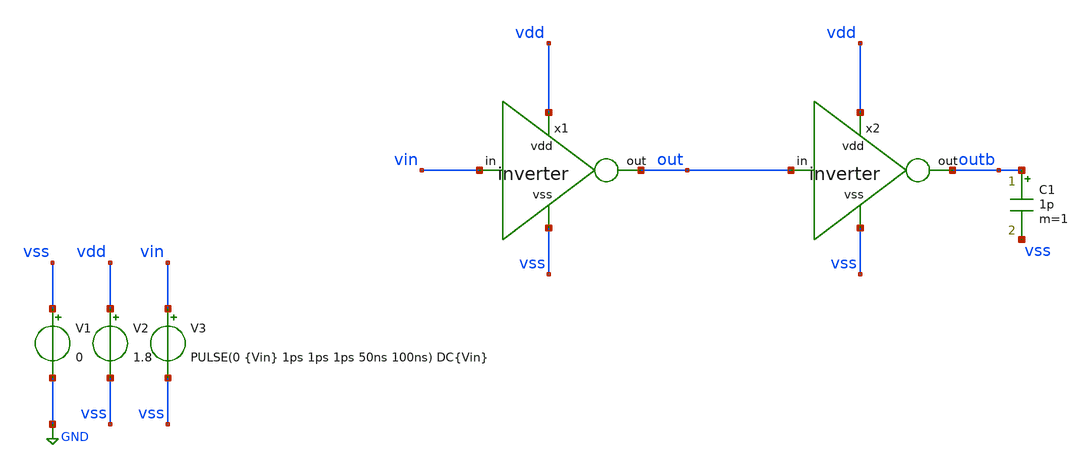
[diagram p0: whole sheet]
** sch_path: track_vlsi/ledesma/sch/tb_inverter.sch
**.subckt tb_inverter
x1 vdd out vin vss inverter
V1 vss GND 0
V2 vdd vss 1.8
V3 vin vss PULSE(0 {Vin} 1ps 1ps 1ps 50ns 100ns) DC{Vin}
x2 vdd outb out vss inverter
C1 outb vss 1p m=1
**** begin user architecture code



* Parametros del circuito
.param Vin = 1.8
.options TEMP = 27.0

* Include
.lib /home/eamta/skywater/skywater-pdk/libraries/sky130_fd_pr_ngspice/latest/models/corners/sky130.lib TT

* Signals to SAVE
.save all  @M.X1.XM1.msky130_fd_pr__nfet_01v8[id] @M.X1.XM1.msky130_fd_pr__nfet_01v8[gm]  @M.X1.XM2.msky130_fd_pr__pfet_01v8[id] @M.X1.XM2.msky130_fd_pr__pfet_01v8[gm]

*simulation
.control
  tran 0.1n 300ns
  setplot tran1
  plot v(out) v(vin)
  write tb_inverter_tran.raw

  reset
  dc V3 0 1.8 0.01
  setplot dc1
  plot v(out) v(vin)
  write tb_inverter_dc.raw

.endc

.end


**** end user architecture code
**.ends

* expanding   symbol:  inverter.sym # of pins=4
** sym_path: track_vlsi/ledesma/sch/inverter.sym
** sch_path: track_vlsi/ledesma/sch/inverter.sch
.subckt inverter vdd out in vss
*.opin out
*.ipin in
*.ipin vdd
*.ipin vss
XM1 out in vss vss sky130_fd_pr__nfet_01v8 L=0.15 W=0.45 nf=1 ad='int((nf+1)/2) * W/nf * 0.29' as='int((nf+2)/2) * W/nf * 0.29'
+ pd='2*int((nf+1)/2) * (W/nf + 0.29)' ps='2*int((nf+2)/2) * (W/nf + 0.29)' nrd='0.29 / W' nrs='0.29 / W'
+ sa=0 sb=0 sd=0 mult=1 m=1
XM2 out in vdd vdd sky130_fd_pr__pfet_01v8 L=0.15 W=0.9 nf=1 ad='int((nf+1)/2) * W/nf * 0.29' as='int((nf+2)/2) * W/nf * 0.29'
+ pd='2*int((nf+1)/2) * (W/nf + 0.29)' ps='2*int((nf+2)/2) * (W/nf + 0.29)' nrd='0.29 / W' nrs='0.29 / W'
+ sa=0 sb=0 sd=0 mult=1 m=1
.ends

.GLOBAL GND
.end
